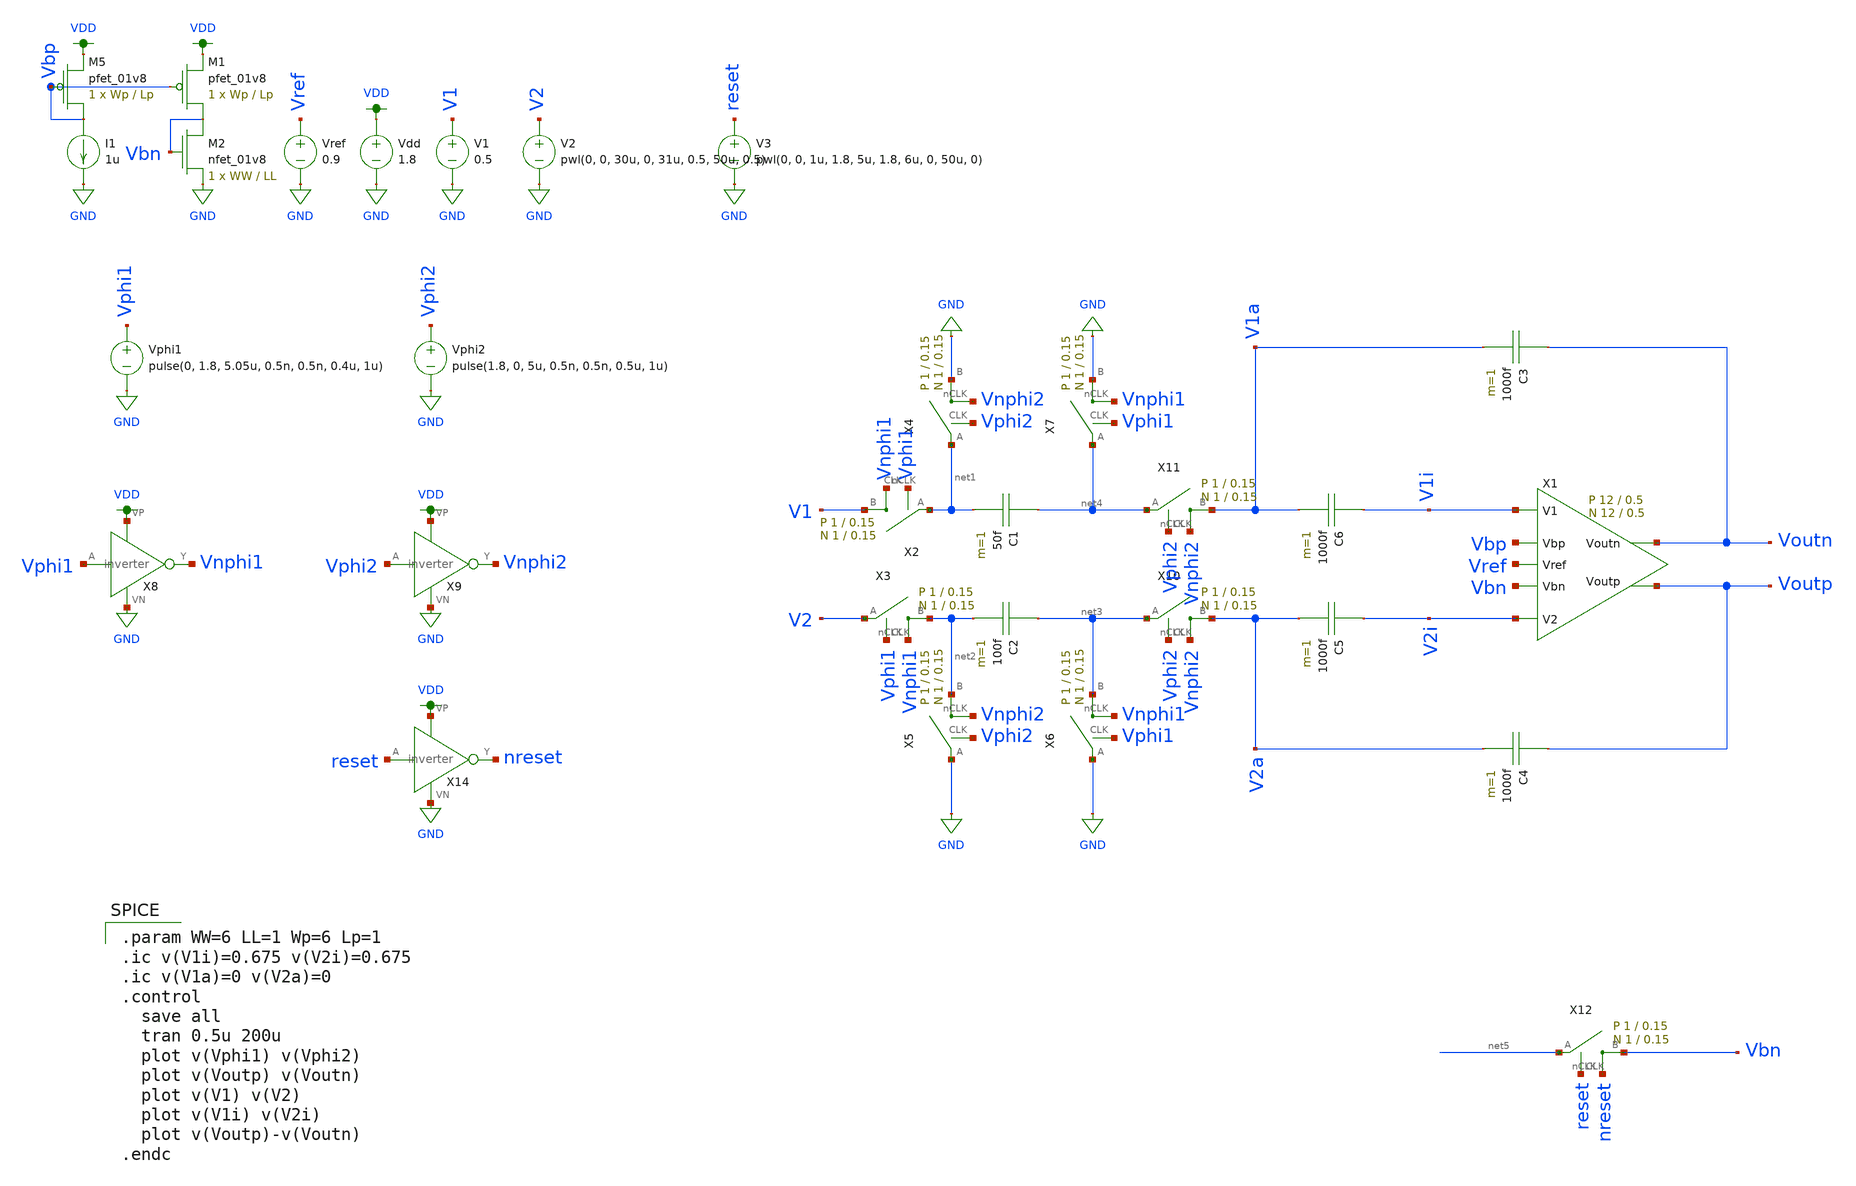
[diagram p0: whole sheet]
** sch_path: schematic/test/FG_integrator_test.sch
**.subckt FG_integrator_test
X1 V1i V2i Voutp Voutn Vbp Vref Vbn fully_differential_sc_amp Wp=12 Lp=0.5 WW=12 LL=0.5
C1 net4 net1 50f m=1
C2 net3 net2 100f m=1
C3 Voutn V1a 1000f m=1
C4 Voutp V2a 1000f m=1
X2 V1 net1 Vphi1 Vnphi1 switch Wp=1 Lp=0.15 WW=1 LL=0.15
X3 net2 V2 Vphi1 Vnphi1 switch Wp=1 Lp=0.15 WW=1 LL=0.15
X4 GND net1 Vphi2 Vnphi2 switch Wp=1 Lp=0.15 WW=1 LL=0.15
X5 net2 GND Vphi2 Vnphi2 switch Wp=1 Lp=0.15 WW=1 LL=0.15
Vdd VDD GND 1.8
V1 V1 GND 0.5
V2 V2 GND pwl(0, 0, 30u, 0, 31u, 0.5, 50u, 0.5)
Vphi1 Vphi1 GND pulse(0, 1.8, 5.05u, 0.5n, 0.5n, 0.4u, 1u)
X8 Vphi1 Vnphi1 VDD GND inverter
Vphi2 Vphi2 GND pulse(1.8, 0, 5u, 0.5n, 0.5n, 0.5u, 1u)
X9 Vphi2 Vnphi2 VDD GND inverter
Vref Vref GND 0.9
XM5 Vbp Vbp VDD VDD sky130_fd_pr__pfet_01v8 L=Lp W=Wp nf=1 ad='int((nf+1)/2) * W/nf * 0.29' as='int((nf+2)/2) * W/nf * 0.29'
+ pd='2*int((nf+1)/2) * (W/nf + 0.29)' ps='2*int((nf+2)/2) * (W/nf + 0.29)' nrd='0.29 / W' nrs='0.29 / W'
+ sa=0 sb=0 sd=0 mult=1 m=1
I1 Vbp GND 1u
XM1 Vbn Vbp VDD VDD sky130_fd_pr__pfet_01v8 L=Lp W=Wp nf=1 ad='int((nf+1)/2) * W/nf * 0.29' as='int((nf+2)/2) * W/nf * 0.29'
+ pd='2*int((nf+1)/2) * (W/nf + 0.29)' ps='2*int((nf+2)/2) * (W/nf + 0.29)' nrd='0.29 / W' nrs='0.29 / W'
+ sa=0 sb=0 sd=0 mult=1 m=1
XM2 Vbn Vbn GND GND sky130_fd_pr__nfet_01v8 L=LL W=WW nf=1 ad='int((nf+1)/2) * W/nf * 0.29' as='int((nf+2)/2) * W/nf * 0.29'
+ pd='2*int((nf+1)/2) * (W/nf + 0.29)' ps='2*int((nf+2)/2) * (W/nf + 0.29)' nrd='0.29 / W' nrs='0.29 / W'
+ sa=0 sb=0 sd=0 mult=1 m=1
X6 net3 GND Vphi1 Vnphi1 switch Wp=1 Lp=0.15 WW=1 LL=0.15
X7 GND net4 Vphi1 Vnphi1 switch Wp=1 Lp=0.15 WW=1 LL=0.15
X10 V2a net3 Vphi2 Vnphi2 switch Wp=1 Lp=0.15 WW=1 LL=0.15
X11 V1a net4 Vphi2 Vnphi2 switch Wp=1 Lp=0.15 WW=1 LL=0.15
X12 Vbn net5 reset nreset switch Wp=1 Lp=0.15 WW=1 LL=0.15
X14 reset nreset VDD GND inverter
V3 reset GND pwl(0, 0, 1u, 1.8, 5u, 1.8, 6u, 0, 50u, 0)
C5 V2i V2a 1000f m=1
C6 V1i V1a 1000f m=1
**** begin user architecture code

.option wnflag=1
.param MC_SWITCH=0.0
.lib /media/qdeng/526448C32060CF5C/skywater/skywater-pdk/libraries/sky130_fd_pr_ngspice/latest/models/sky130.lib.spice tt


.param WW=6 LL=1 Wp=6 Lp=1
.ic v(V1i)=0.675 v(V2i)=0.675
.ic v(V1a)=0 v(V2a)=0
.control
  save all
  tran 0.5u 200u
  plot v(Vphi1) v(Vphi2)
  plot v(Voutp) v(Voutn)
  plot v(V1) v(V2)
  plot v(V1i) v(V2i)
  plot v(Voutp)-v(Voutn)
.endc

**** end user architecture code
**.ends

* expanding   symbol:
*+  /home/madvlsi/Documents/MADVLSI-Final_Project/schematic/fully_differential_sc_amp.sym # of pins=7
** sym_path: schematic/archive/fully_differential_sc_amp.sym
** sch_path: schematic/archive/fully_differential_sc_amp.sch
.subckt fully_differential_sc_amp V1 V2 Voutp Voutn Vbp Vref Vbn  Wp=1 Lp=0.15 WW=1 LL=0.15
*.ipin V1
*.ipin V2
*.ipin Vbp
*.ipin Vbn
*.ipin Vref
*.iopin Voutp
*.iopin Voutn
XM1a net2 V1 GND GND sky130_fd_pr__nfet_01v8 L=LL W=WW nf=1 ad='int((nf+1)/2) * W/nf * 0.29' as='int((nf+2)/2) * W/nf * 0.29'
+ pd='2*int((nf+1)/2) * (W/nf + 0.29)' ps='2*int((nf+2)/2) * (W/nf + 0.29)' nrd='0.29 / W' nrs='0.29 / W'
+ sa=0 sb=0 sd=0 mult=1 m=1
XM1b Voutn V1 GND GND sky130_fd_pr__nfet_01v8 L=LL W=WW nf=1 ad='int((nf+1)/2) * W/nf * 0.29' as='int((nf+2)/2) * W/nf * 0.29'
+ pd='2*int((nf+1)/2) * (W/nf + 0.29)' ps='2*int((nf+2)/2) * (W/nf + 0.29)' nrd='0.29 / W' nrs='0.29 / W'
+ sa=0 sb=0 sd=0 mult=1 m=1
XM2b Voutp V2 GND GND sky130_fd_pr__nfet_01v8 L=LL W=WW nf=1 ad='int((nf+1)/2) * W/nf * 0.29' as='int((nf+2)/2) * W/nf * 0.29'
+ pd='2*int((nf+1)/2) * (W/nf + 0.29)' ps='2*int((nf+2)/2) * (W/nf + 0.29)' nrd='0.29 / W' nrs='0.29 / W'
+ sa=0 sb=0 sd=0 mult=1 m=1
XM2a net2 V2 GND GND sky130_fd_pr__nfet_01v8 L=LL W=WW nf=1 ad='int((nf+1)/2) * W/nf * 0.29' as='int((nf+2)/2) * W/nf * 0.29'
+ pd='2*int((nf+1)/2) * (W/nf + 0.29)' ps='2*int((nf+2)/2) * (W/nf + 0.29)' nrd='0.29 / W' nrs='0.29 / W'
+ sa=0 sb=0 sd=0 mult=1 m=1
XMb net2 Vbp VDD VDD sky130_fd_pr__pfet_01v8 L=Lp W=Wp nf=1 ad='int((nf+1)/2) * W/nf * 0.29' as='int((nf+2)/2) * W/nf * 0.29'
+ pd='2*int((nf+1)/2) * (W/nf + 0.29)' ps='2*int((nf+2)/2) * (W/nf + 0.29)' nrd='0.29 / W' nrs='0.29 / W'
+ sa=0 sb=0 sd=0 mult=1 m=1
C2b net2 V2 1600f m=1
C2a net2 V1 1600f m=1
XM1 GND V2 net1 GND sky130_fd_pr__nfet_01v8 L=LL W=WW nf=1 ad='int((nf+1)/2) * W/nf * 0.29' as='int((nf+2)/2) * W/nf * 0.29'
+ pd='2*int((nf+1)/2) * (W/nf + 0.29)' ps='2*int((nf+2)/2) * (W/nf + 0.29)' nrd='0.29 / W' nrs='0.29 / W'
+ sa=0 sb=0 sd=0 mult=1 m=1
XM2 GND V1 net1 GND sky130_fd_pr__nfet_01v8 L=LL W=WW nf=1 ad='int((nf+1)/2) * W/nf * 0.29' as='int((nf+2)/2) * W/nf * 0.29'
+ pd='2*int((nf+1)/2) * (W/nf + 0.29)' ps='2*int((nf+2)/2) * (W/nf + 0.29)' nrd='0.29 / W' nrs='0.29 / W'
+ sa=0 sb=0 sd=0 mult=1 m=1
XMb1 VDD net4 net5 VDD sky130_fd_pr__pfet_01v8 L=Lp W=Wp nf=1 ad='int((nf+1)/2) * W/nf * 0.29' as='int((nf+2)/2) * W/nf * 0.29'
+ pd='2*int((nf+1)/2) * (W/nf + 0.29)' ps='2*int((nf+2)/2) * (W/nf + 0.29)' nrd='0.29 / W' nrs='0.29 / W'
+ sa=0 sb=0 sd=0 mult=1 m=1
XMb2 VDD net4 net1 VDD sky130_fd_pr__pfet_01v8 L=Lp W=Wp nf=1 ad='int((nf+1)/2) * W/nf * 0.29' as='int((nf+2)/2) * W/nf * 0.29'
+ pd='2*int((nf+1)/2) * (W/nf + 0.29)' ps='2*int((nf+2)/2) * (W/nf + 0.29)' nrd='0.29 / W' nrs='0.29 / W'
+ sa=0 sb=0 sd=0 mult=1 m=1
XMb4 VDD net4 net6 VDD sky130_fd_pr__pfet_01v8 L=Lp W=Wp nf=1 ad='int((nf+1)/2) * W/nf * 0.29' as='int((nf+2)/2) * W/nf * 0.29'
+ pd='2*int((nf+1)/2) * (W/nf + 0.29)' ps='2*int((nf+2)/2) * (W/nf + 0.29)' nrd='0.29 / W' nrs='0.29 / W'
+ sa=0 sb=0 sd=0 mult=1 m=1
XMb5 net7 net4 VDD VDD sky130_fd_pr__pfet_01v8 L=Lp W=Wp nf=1 ad='int((nf+1)/2) * W/nf * 0.29' as='int((nf+2)/2) * W/nf * 0.29'
+ pd='2*int((nf+1)/2) * (W/nf + 0.29)' ps='2*int((nf+2)/2) * (W/nf + 0.29)' nrd='0.29 / W' nrs='0.29 / W'
+ sa=0 sb=0 sd=0 mult=1 m=1
XM3 net3 Vbn GND GND sky130_fd_pr__nfet_01v8 L=LL W=WW nf=1 ad='int((nf+1)/2) * W/nf * 0.29' as='int((nf+2)/2) * W/nf * 0.29'
+ pd='2*int((nf+1)/2) * (W/nf + 0.29)' ps='2*int((nf+2)/2) * (W/nf + 0.29)' nrd='0.29 / W' nrs='0.29 / W'
+ sa=0 sb=0 sd=0 mult=1 m=1
XM4 VDD net1 net3 GND sky130_fd_pr__nfet_01v8 L=LL W=WW nf=1 ad='int((nf+1)/2) * W/nf * 0.29' as='int((nf+2)/2) * W/nf * 0.29'
+ pd='2*int((nf+1)/2) * (W/nf + 0.29)' ps='2*int((nf+2)/2) * (W/nf + 0.29)' nrd='0.29 / W' nrs='0.29 / W'
+ sa=0 sb=0 sd=0 mult=1 m=1
XM5 net3 Vref net4 GND sky130_fd_pr__nfet_01v8 L=LL W=WW nf=1 ad='int((nf+1)/2) * W/nf * 0.29' as='int((nf+2)/2) * W/nf * 0.29'
+ pd='2*int((nf+1)/2) * (W/nf + 0.29)' ps='2*int((nf+2)/2) * (W/nf + 0.29)' nrd='0.29 / W' nrs='0.29 / W'
+ sa=0 sb=0 sd=0 mult=1 m=1
XMb6 net5 net4 Voutn VDD sky130_fd_pr__pfet_01v8 L=Lp W=Wp nf=1 ad='int((nf+1)/2) * W/nf * 0.29' as='int((nf+2)/2) * W/nf * 0.29'
+ pd='2*int((nf+1)/2) * (W/nf + 0.29)' ps='2*int((nf+2)/2) * (W/nf + 0.29)' nrd='0.29 / W' nrs='0.29 / W'
+ sa=0 sb=0 sd=0 mult=1 m=1
XMb7 net6 net4 Voutp VDD sky130_fd_pr__pfet_01v8 L=Lp W=Wp nf=1 ad='int((nf+1)/2) * W/nf * 0.29' as='int((nf+2)/2) * W/nf * 0.29'
+ pd='2*int((nf+1)/2) * (W/nf + 0.29)' ps='2*int((nf+2)/2) * (W/nf + 0.29)' nrd='0.29 / W' nrs='0.29 / W'
+ sa=0 sb=0 sd=0 mult=1 m=1
XMb8 net4 net4 net7 VDD sky130_fd_pr__pfet_01v8 L=Lp W=Wp nf=1 ad='int((nf+1)/2) * W/nf * 0.29' as='int((nf+2)/2) * W/nf * 0.29'
+ pd='2*int((nf+1)/2) * (W/nf + 0.29)' ps='2*int((nf+2)/2) * (W/nf + 0.29)' nrd='0.29 / W' nrs='0.29 / W'
+ sa=0 sb=0 sd=0 mult=1 m=1
.ends


* expanding   symbol:  /home/madvlsi/Documents/MADVLSI-Final_Project/schematic/switch.sym # of
*+ pins=4
** sym_path: schematic/switch.sym
** sch_path: schematic/switch.sch
.subckt switch B A CLK nCLK  Wp=1 Lp=0.15 WW=1 LL=0.15
*.iopin B
*.iopin A
*.ipin CLK
*.ipin nCLK
*.ipin CLK
*.ipin CLK
*.ipin nCLK
*.ipin nCLK
XM1 A CLK B GND sky130_fd_pr__nfet_01v8 L={LL} W={WW} nf=1 ad='int((nf+1)/2) * W/nf * 0.29' as='int((nf+2)/2) * W/nf * 0.29'
+ pd='2*int((nf+1)/2) * (W/nf + 0.29)' ps='2*int((nf+2)/2) * (W/nf + 0.29)' nrd='0.29 / W' nrs='0.29 / W'
+ sa=0 sb=0 sd=0 mult=1 m=1
XM2 A nCLK B VDD sky130_fd_pr__pfet_01v8 L={Lp} W={Wp} nf=1 ad='int((nf+1)/2) * W/nf * 0.29' as='int((nf+2)/2) * W/nf * 0.29'
+ pd='2*int((nf+1)/2) * (W/nf + 0.29)' ps='2*int((nf+2)/2) * (W/nf + 0.29)' nrd='0.29 / W' nrs='0.29 / W'
+ sa=0 sb=0 sd=0 mult=1 m=1
XM3 B CLK B VDD sky130_fd_pr__pfet_01v8 L={Lp} W={Wp/2} nf=1 ad='int((nf+1)/2) * W/nf * 0.29' as='int((nf+2)/2) * W/nf * 0.29'
+ pd='2*int((nf+1)/2) * (W/nf + 0.29)' ps='2*int((nf+2)/2) * (W/nf + 0.29)' nrd='0.29 / W' nrs='0.29 / W'
+ sa=0 sb=0 sd=0 mult=1 m=1
XM4 A CLK A VDD sky130_fd_pr__pfet_01v8 L={Lp} W={Wp/2} nf=1 ad='int((nf+1)/2) * W/nf * 0.29' as='int((nf+2)/2) * W/nf * 0.29'
+ pd='2*int((nf+1)/2) * (W/nf + 0.29)' ps='2*int((nf+2)/2) * (W/nf + 0.29)' nrd='0.29 / W' nrs='0.29 / W'
+ sa=0 sb=0 sd=0 mult=1 m=1
XM5 B nCLK B GND sky130_fd_pr__nfet_01v8 L={LL} W={WW/2} nf=1 ad='int((nf+1)/2) * W/nf * 0.29' as='int((nf+2)/2) * W/nf * 0.29'
+ pd='2*int((nf+1)/2) * (W/nf + 0.29)' ps='2*int((nf+2)/2) * (W/nf + 0.29)' nrd='0.29 / W' nrs='0.29 / W'
+ sa=0 sb=0 sd=0 mult=1 m=1
XM6 A nCLK A GND sky130_fd_pr__nfet_01v8 L={LL} W={WW/2} nf=1 ad='int((nf+1)/2) * W/nf * 0.29' as='int((nf+2)/2) * W/nf * 0.29'
+ pd='2*int((nf+1)/2) * (W/nf + 0.29)' ps='2*int((nf+2)/2) * (W/nf + 0.29)' nrd='0.29 / W' nrs='0.29 / W'
+ sa=0 sb=0 sd=0 mult=1 m=1
.ends


* expanding   symbol:  /home/madvlsi/Documents/MADVLSI-Final_Project/schematic/inverter.sym # of
*+ pins=4
** sym_path: schematic/inverter.sym
** sch_path: schematic/inverter.sch
.subckt inverter A Y VP VN
*.opin Y
*.ipin A
*.iopin VP
*.iopin VN
XM3 Y A VP VDD sky130_fd_pr__pfet_01v8 L={Lp} W={Wp} nf=1 ad='int((nf+1)/2) * W/nf * 0.29' as='int((nf+2)/2) * W/nf * 0.29'
+ pd='2*int((nf+1)/2) * (W/nf + 0.29)' ps='2*int((nf+2)/2) * (W/nf + 0.29)' nrd='0.29 / W' nrs='0.29 / W'
+ sa=0 sb=0 sd=0 mult=1 m=1
XM4 Y A VP VDD sky130_fd_pr__pfet_01v8 L={Lp} W={Wp} nf=1 ad='int((nf+1)/2) * W/nf * 0.29' as='int((nf+2)/2) * W/nf * 0.29'
+ pd='2*int((nf+1)/2) * (W/nf + 0.29)' ps='2*int((nf+2)/2) * (W/nf + 0.29)' nrd='0.29 / W' nrs='0.29 / W'
+ sa=0 sb=0 sd=0 mult=1 m=1
XM5 Y A VN GND sky130_fd_pr__nfet_01v8 L={Lp} W={Wp} nf=1 ad='int((nf+1)/2) * W/nf * 0.29' as='int((nf+2)/2) * W/nf * 0.29'
+ pd='2*int((nf+1)/2) * (W/nf + 0.29)' ps='2*int((nf+2)/2) * (W/nf + 0.29)' nrd='0.29 / W' nrs='0.29 / W'
+ sa=0 sb=0 sd=0 mult=1 m=1
.ends

.GLOBAL GND
.GLOBAL VDD
.end
